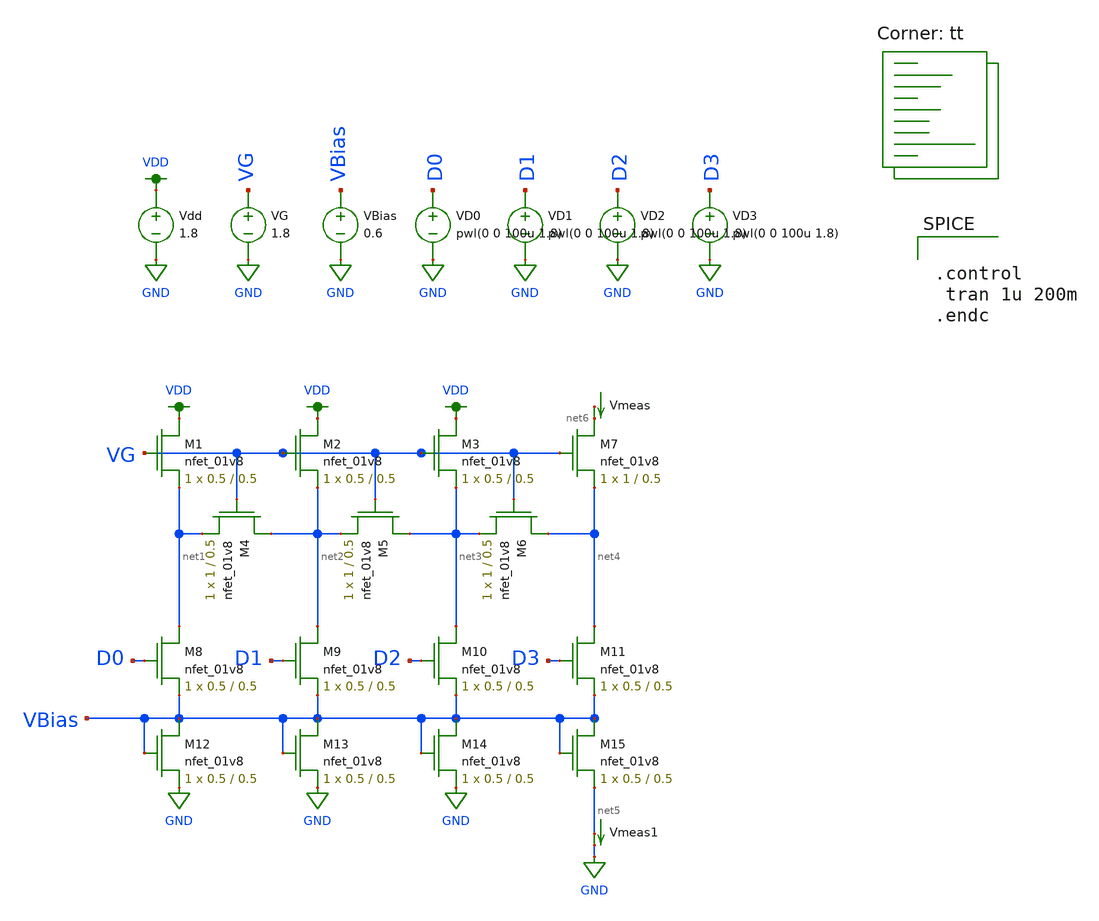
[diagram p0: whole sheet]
** sch_path: MADVLSI_MP3/TRIAL2.sch
**.subckt TRIAL2
XM1 VDD VG net1 GND sky130_fd_pr__nfet_01v8 L=0.5 W=0.5 nf=1 ad='int((nf+1)/2) * W/nf * 0.29' as='int((nf+2)/2) * W/nf * 0.29'
+ pd='2*int((nf+1)/2) * (W/nf + 0.29)' ps='2*int((nf+2)/2) * (W/nf + 0.29)' nrd='0.29 / W' nrs='0.29 / W'
+ sa=0 sb=0 sd=0 mult=1 m=1
XM2 VDD VG net2 GND sky130_fd_pr__nfet_01v8 L=0.5 W=0.5 nf=1 ad='int((nf+1)/2) * W/nf * 0.29' as='int((nf+2)/2) * W/nf * 0.29'
+ pd='2*int((nf+1)/2) * (W/nf + 0.29)' ps='2*int((nf+2)/2) * (W/nf + 0.29)' nrd='0.29 / W' nrs='0.29 / W'
+ sa=0 sb=0 sd=0 mult=1 m=1
XM3 VDD VG net3 GND sky130_fd_pr__nfet_01v8 L=0.5 W=0.5 nf=1 ad='int((nf+1)/2) * W/nf * 0.29' as='int((nf+2)/2) * W/nf * 0.29'
+ pd='2*int((nf+1)/2) * (W/nf + 0.29)' ps='2*int((nf+2)/2) * (W/nf + 0.29)' nrd='0.29 / W' nrs='0.29 / W'
+ sa=0 sb=0 sd=0 mult=1 m=1
XM4 net2 VG net1 GND sky130_fd_pr__nfet_01v8 L=0.5 W=1 nf=1 ad='int((nf+1)/2) * W/nf * 0.29' as='int((nf+2)/2) * W/nf * 0.29'
+ pd='2*int((nf+1)/2) * (W/nf + 0.29)' ps='2*int((nf+2)/2) * (W/nf + 0.29)' nrd='0.29 / W' nrs='0.29 / W'
+ sa=0 sb=0 sd=0 mult=1 m=1
XM5 net3 VG net2 GND sky130_fd_pr__nfet_01v8 L=0.5 W=1 nf=1 ad='int((nf+1)/2) * W/nf * 0.29' as='int((nf+2)/2) * W/nf * 0.29'
+ pd='2*int((nf+1)/2) * (W/nf + 0.29)' ps='2*int((nf+2)/2) * (W/nf + 0.29)' nrd='0.29 / W' nrs='0.29 / W'
+ sa=0 sb=0 sd=0 mult=1 m=1
XM6 net4 VG net3 GND sky130_fd_pr__nfet_01v8 L=0.5 W=1 nf=1 ad='int((nf+1)/2) * W/nf * 0.29' as='int((nf+2)/2) * W/nf * 0.29'
+ pd='2*int((nf+1)/2) * (W/nf + 0.29)' ps='2*int((nf+2)/2) * (W/nf + 0.29)' nrd='0.29 / W' nrs='0.29 / W'
+ sa=0 sb=0 sd=0 mult=1 m=1
XM7 net6 VG net4 GND sky130_fd_pr__nfet_01v8 L=0.5 W=1 nf=1 ad='int((nf+1)/2) * W/nf * 0.29' as='int((nf+2)/2) * W/nf * 0.29'
+ pd='2*int((nf+1)/2) * (W/nf + 0.29)' ps='2*int((nf+2)/2) * (W/nf + 0.29)' nrd='0.29 / W' nrs='0.29 / W'
+ sa=0 sb=0 sd=0 mult=1 m=1
XM8 net1 D0 VBias GND sky130_fd_pr__nfet_01v8 L=0.5 W=0.5 nf=1 ad='int((nf+1)/2) * W/nf * 0.29' as='int((nf+2)/2) * W/nf * 0.29'
+ pd='2*int((nf+1)/2) * (W/nf + 0.29)' ps='2*int((nf+2)/2) * (W/nf + 0.29)' nrd='0.29 / W' nrs='0.29 / W'
+ sa=0 sb=0 sd=0 mult=1 m=1
XM9 net2 D1 VBias GND sky130_fd_pr__nfet_01v8 L=0.5 W=0.5 nf=1 ad='int((nf+1)/2) * W/nf * 0.29' as='int((nf+2)/2) * W/nf * 0.29'
+ pd='2*int((nf+1)/2) * (W/nf + 0.29)' ps='2*int((nf+2)/2) * (W/nf + 0.29)' nrd='0.29 / W' nrs='0.29 / W'
+ sa=0 sb=0 sd=0 mult=1 m=1
XM10 net3 D2 VBias GND sky130_fd_pr__nfet_01v8 L=0.5 W=0.5 nf=1 ad='int((nf+1)/2) * W/nf * 0.29' as='int((nf+2)/2) * W/nf * 0.29'
+ pd='2*int((nf+1)/2) * (W/nf + 0.29)' ps='2*int((nf+2)/2) * (W/nf + 0.29)' nrd='0.29 / W' nrs='0.29 / W'
+ sa=0 sb=0 sd=0 mult=1 m=1
XM11 net4 D3 VBias GND sky130_fd_pr__nfet_01v8 L=0.5 W=0.5 nf=1 ad='int((nf+1)/2) * W/nf * 0.29' as='int((nf+2)/2) * W/nf * 0.29'
+ pd='2*int((nf+1)/2) * (W/nf + 0.29)' ps='2*int((nf+2)/2) * (W/nf + 0.29)' nrd='0.29 / W' nrs='0.29 / W'
+ sa=0 sb=0 sd=0 mult=1 m=1
Vmeas net7 net6 0
.save i(vmeas)
XM12 VBias VBias GND GND sky130_fd_pr__nfet_01v8 L=0.5 W=0.5 nf=1 ad='int((nf+1)/2) * W/nf * 0.29' as='int((nf+2)/2) * W/nf * 0.29'
+ pd='2*int((nf+1)/2) * (W/nf + 0.29)' ps='2*int((nf+2)/2) * (W/nf + 0.29)' nrd='0.29 / W' nrs='0.29 / W'
+ sa=0 sb=0 sd=0 mult=1 m=1
XM13 VBias VBias GND GND sky130_fd_pr__nfet_01v8 L=0.5 W=0.5 nf=1 ad='int((nf+1)/2) * W/nf * 0.29' as='int((nf+2)/2) * W/nf * 0.29'
+ pd='2*int((nf+1)/2) * (W/nf + 0.29)' ps='2*int((nf+2)/2) * (W/nf + 0.29)' nrd='0.29 / W' nrs='0.29 / W'
+ sa=0 sb=0 sd=0 mult=1 m=1
XM14 VBias VBias GND GND sky130_fd_pr__nfet_01v8 L=0.5 W=0.5 nf=1 ad='int((nf+1)/2) * W/nf * 0.29' as='int((nf+2)/2) * W/nf * 0.29'
+ pd='2*int((nf+1)/2) * (W/nf + 0.29)' ps='2*int((nf+2)/2) * (W/nf + 0.29)' nrd='0.29 / W' nrs='0.29 / W'
+ sa=0 sb=0 sd=0 mult=1 m=1
XM15 VBias VBias net5 GND sky130_fd_pr__nfet_01v8 L=0.5 W=0.5 nf=1 ad='int((nf+1)/2) * W/nf * 0.29' as='int((nf+2)/2) * W/nf * 0.29'
+ pd='2*int((nf+1)/2) * (W/nf + 0.29)' ps='2*int((nf+2)/2) * (W/nf + 0.29)' nrd='0.29 / W' nrs='0.29 / W'
+ sa=0 sb=0 sd=0 mult=1 m=1
Vmeas1 net5 GND 0
.save i(vmeas1)
Vdd VDD GND 1.8
VG VG GND 1.8
VBias VBias GND 0.6
VD0 D0 GND pwl(0 0 100u 1.8)
VD1 D1 GND pwl(0 0 100u 1.8)
VD2 D2 GND pwl(0 0 100u 1.8)
VD3 D3 GND pwl(0 0 100u 1.8)
**** begin user architecture code


.control
 tran 1u 200m
.endc



.lib $::SKYWATER_MODELS/sky130.lib.spice tt
**** end user architecture code
**.ends
.GLOBAL GND
.GLOBAL VDD
.end
